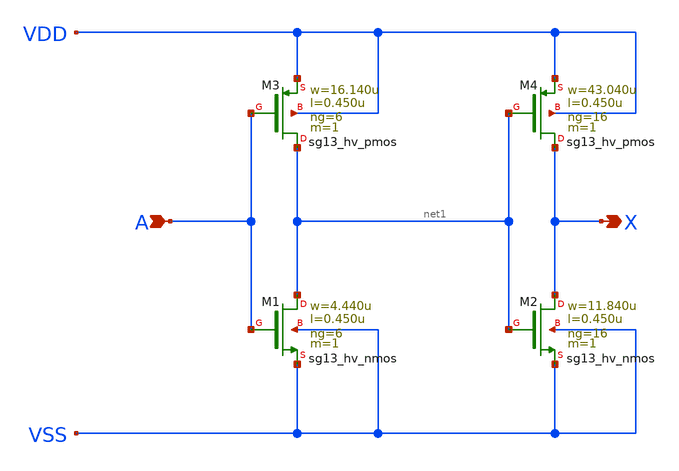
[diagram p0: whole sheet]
** sch_path: ihp-sg13g2/libs.ref/sg13g2_stdcell_hv/sch/xschem/sg13g2_hv_buf_16.sch
* Copyright 2023 IHP PDK Authors
* Licensed under the Apache License, Version 2.0 (the "License");
* you may not use this file except in compliance with the License.
* You may obtain a copy of the License at
* https://www.apache.org/licenses/LICENSE-2.0
* Unless required by applicable law or agreed to in writing, software
* distributed under the License is distributed on an "AS IS" BASIS,
* WITHOUT WARRANTIES OR CONDITIONS OF ANY KIND, either express or implied.
* See the License for the specific language governing permissions and
* limitations under the License.
**.subckt sg13g2_hv_buf_16 A X
*.ipin A
*.opin X
XM1 net1 A VSS VSS sg13_hv_nmos w=4.440u l=0.450u ng=6 m=1 mm_ok=1
XM2 X net1 VSS VSS sg13_hv_nmos w=11.840u l=0.450u ng=16 m=1 mm_ok=1
XM3 net1 A VDD VDD sg13_hv_pmos w=16.140u l=0.450u ng=6 m=1 mm_ok=1
XM4 X net1 VDD VDD sg13_hv_pmos w=43.040u l=0.450u ng=16 m=1 mm_ok=1
**.ends
.end
